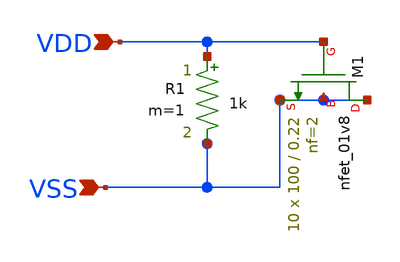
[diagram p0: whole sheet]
** sch_path: design/LELO_SVOD_SKY130A/LELO_CAP.sch
**.subckt LELO_CAP VSS VDD
*.ipin VSS
*.ipin VDD
XM1 VSS VDD VSS VSS sky130_fd_pr__nfet_01v8 L=0.22 W=100 nf=2 ad='int((nf+1)/2) * W/nf * 0.29' as='int((nf+2)/2) * W/nf * 0.29'
+ pd='2*int((nf+1)/2) * (W/nf + 0.29)' ps='2*int((nf+2)/2) * (W/nf + 0.29)' nrd='0.29 / W' nrs='0.29 / W'
+ sa=0 sb=0 sd=0 mult=10 m=10
R1 VDD VSS 1k m=1
**.ends
.end
